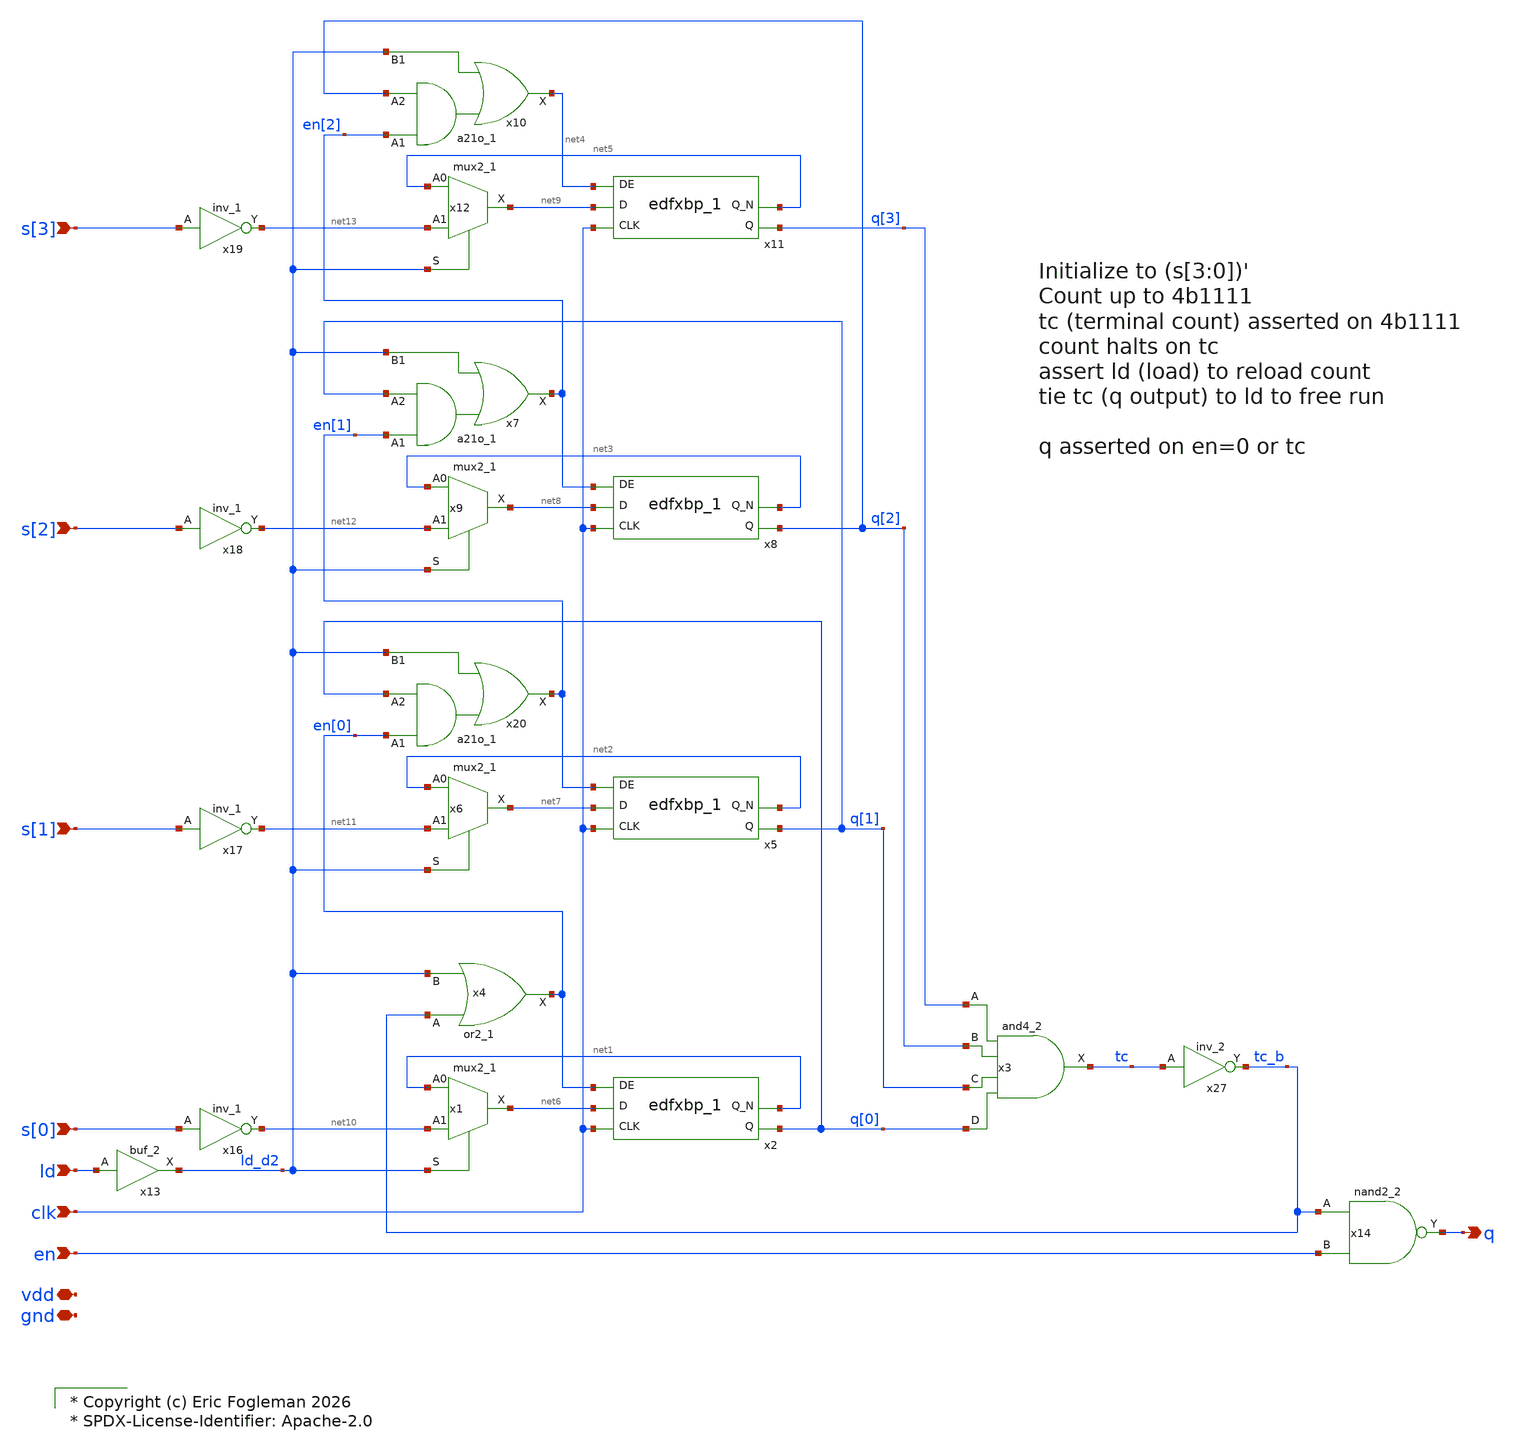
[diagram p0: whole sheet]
** sch_path: xschem/ejf_pll96_sdiv_s.sch

* Copyright (c) Eric Fogleman 2026
* SPDX-License-Identifier: Apache-2.0

**.subckt ejf_pll96_sdiv_s s[1] s[2] s[3] clk q ld s[0] en vdd gnd
*.ipin s[1]
*.ipin s[2]
*.ipin s[3]
*.ipin clk
*.opin q
*.ipin ld
*.ipin s[0]
*.ipin en
*.iopin vdd
*.iopin gnd
x3 q[3] q[2] q[1] q[0] gnd gnd vdd vdd tc sky130_fd_sc_ls__and4_2
x27 tc gnd gnd vdd vdd tc_b sky130_fd_sc_ls__inv_2
x2 clk net6 en[0] gnd gnd vdd vdd q[0] net1 sky130_fd_sc_ls__edfxbp_1
x1 net1 net10 ld_d2 gnd gnd vdd vdd net6 sky130_fd_sc_ls__mux2_1
x5 clk net7 en[1] gnd gnd vdd vdd q[1] net2 sky130_fd_sc_ls__edfxbp_1
x6 net2 net11 ld_d2 gnd gnd vdd vdd net7 sky130_fd_sc_ls__mux2_1
x8 clk net8 en[2] gnd gnd vdd vdd q[2] net3 sky130_fd_sc_ls__edfxbp_1
x9 net3 net12 ld_d2 gnd gnd vdd vdd net8 sky130_fd_sc_ls__mux2_1
x11 clk net9 net4 gnd gnd vdd vdd q[3] net5 sky130_fd_sc_ls__edfxbp_1
x12 net5 net13 ld_d2 gnd gnd vdd vdd net9 sky130_fd_sc_ls__mux2_1
x4 tc_b ld_d2 gnd gnd vdd vdd en[0] sky130_fd_sc_ls__or2_1
x16 s[0] gnd gnd vdd vdd net10 sky130_fd_sc_ls__inv_1
x20 en[0] q[0] ld_d2 gnd gnd vdd vdd en[1] sky130_fd_sc_ls__a21o_1
x7 en[1] q[1] ld_d2 gnd gnd vdd vdd en[2] sky130_fd_sc_ls__a21o_1
x10 en[2] q[2] ld_d2 gnd gnd vdd vdd net4 sky130_fd_sc_ls__a21o_1
x13 ld gnd gnd vdd vdd ld_d2 sky130_fd_sc_ls__buf_2
x17 s[1] gnd gnd vdd vdd net11 sky130_fd_sc_ls__inv_1
x18 s[2] gnd gnd vdd vdd net12 sky130_fd_sc_ls__inv_1
x19 s[3] gnd gnd vdd vdd net13 sky130_fd_sc_ls__inv_1
x14 tc_b en gnd gnd vdd vdd q sky130_fd_sc_ls__nand2_2
**.ends
.end
